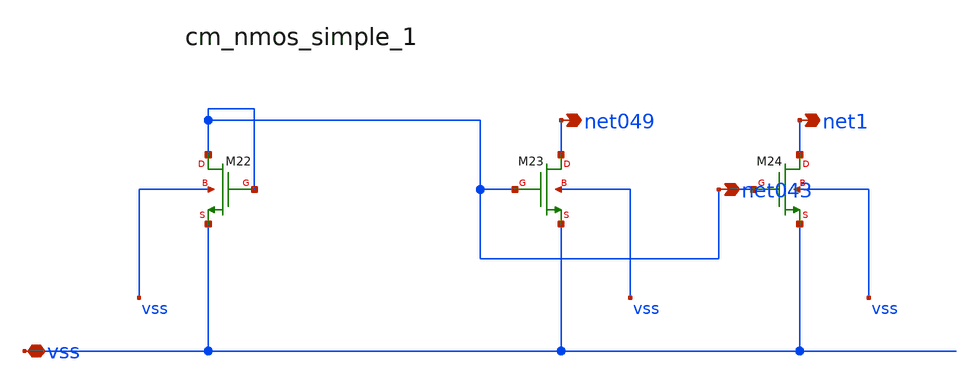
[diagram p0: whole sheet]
** sch_path: analog-db/raw/amp_010_peng_acbc/hier/blocks/cm_nmos_simple_1.sch
**.subckt cm_nmos_simple_1 vss net043 net049 net1
*.iopin vss
*.opin net043
*.opin net049
*.opin net1
XM22 net043 net043 vss vss sg13_lv_nmos w=x_dut_xm22_w l=x_dut_xm22_l ng=1 m=x_dut_xm22_m
XM23 net049 net043 vss vss sg13_lv_nmos w=x_dut_xm23_w l=x_dut_xm23_l ng=1 m=x_dut_xm23_m
XM24 net1 net043 vss vss sg13_lv_nmos w=x_dut_xm24_w l=x_dut_xm24_l ng=1 m=x_dut_xm24_m
**.ends
.end
